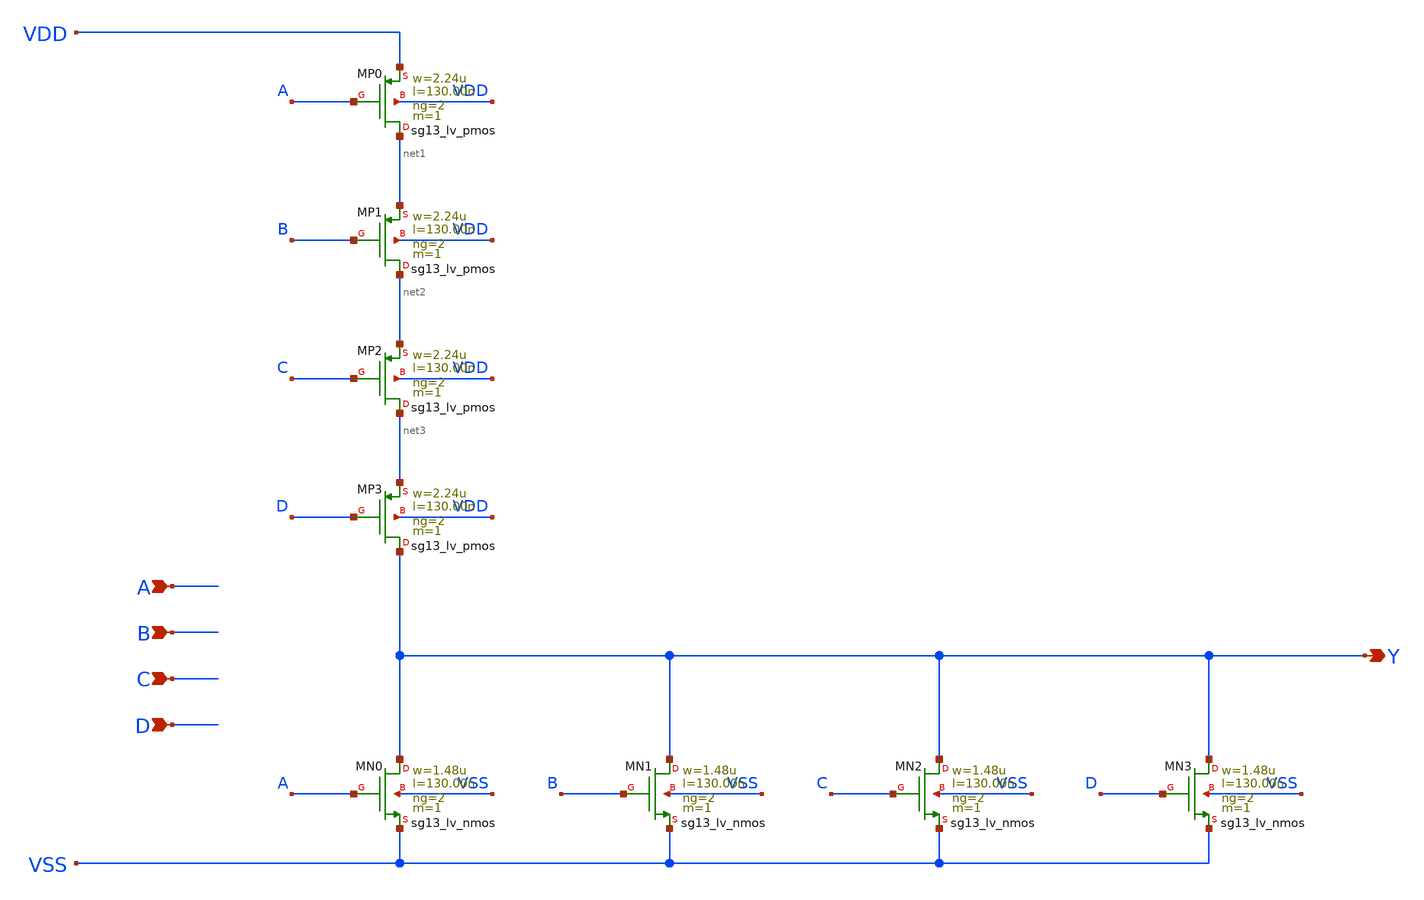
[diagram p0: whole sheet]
** sch_path: outputs/sg13g2_cells/cells/sg13g2_nor4_2/sg13g2_nor4_2.sch
**.subckt sg13g2_nor4_2 A B C D Y
*.ipin A
*.ipin B
*.ipin C
*.ipin D
*.opin Y
XMN0 Y A VSS VSS sg13_lv_nmos w=1.48u l=130.00n ng=2 m=1 mm_ok=1
XMN3 Y D VSS VSS sg13_lv_nmos w=1.48u l=130.00n ng=2 m=1 mm_ok=1
XMN1 Y B VSS VSS sg13_lv_nmos w=1.48u l=130.00n ng=2 m=1 mm_ok=1
XMN2 Y C VSS VSS sg13_lv_nmos w=1.48u l=130.00n ng=2 m=1 mm_ok=1
XMP0 net1 A VDD VDD sg13_lv_pmos w=2.24u l=130.00n ng=2 m=1 mm_ok=1
XMP1 net2 B net1 VDD sg13_lv_pmos w=2.24u l=130.00n ng=2 m=1 mm_ok=1
XMP2 net3 C net2 VDD sg13_lv_pmos w=2.24u l=130.00n ng=2 m=1 mm_ok=1
XMP3 Y D net3 VDD sg13_lv_pmos w=2.24u l=130.00n ng=2 m=1 mm_ok=1
**.ends
.end
